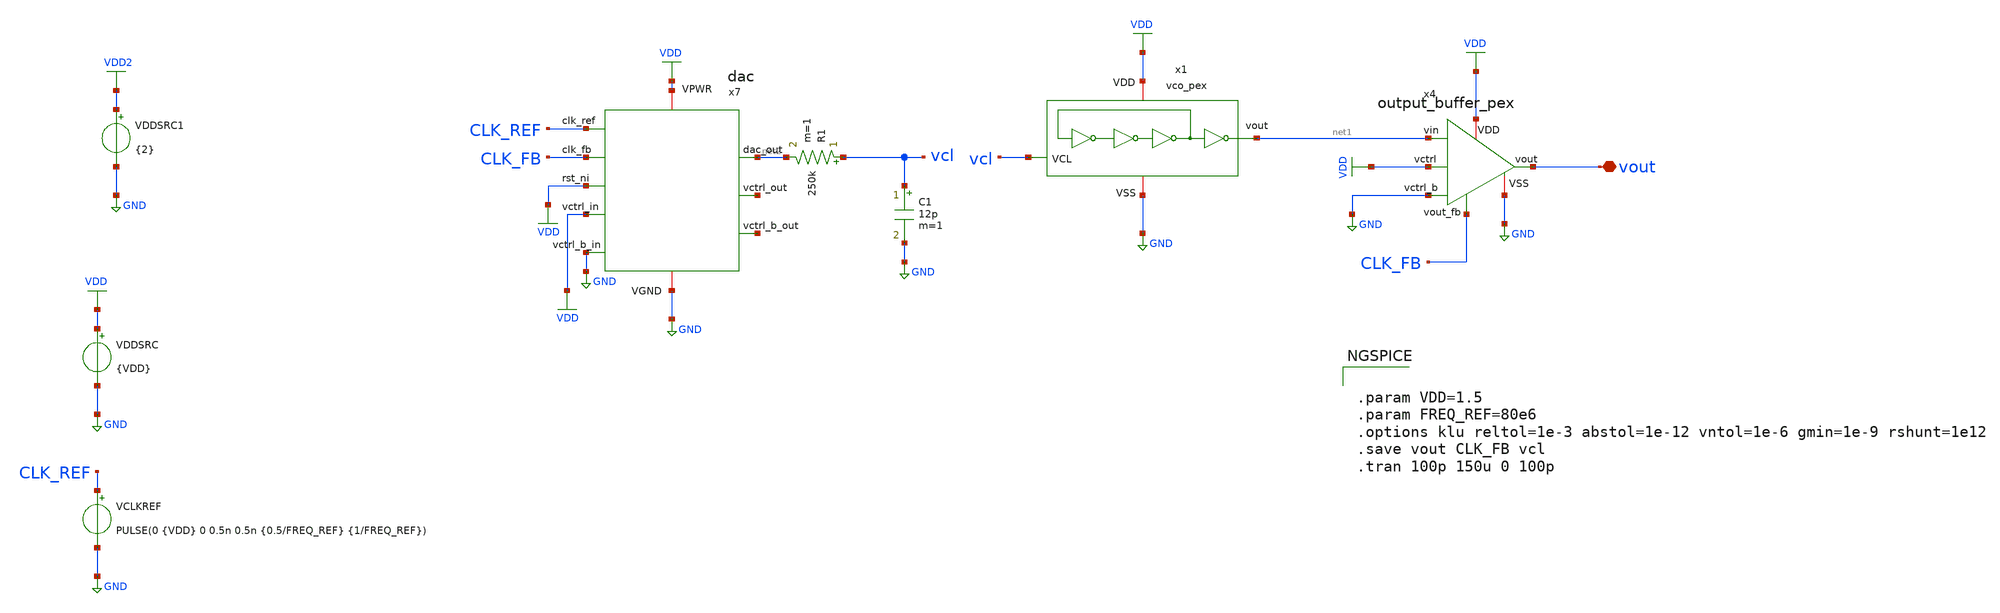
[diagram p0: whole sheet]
** sch_path: macros/heichips26_ook_top/macros/ook_analog_system/testbenches/xschem/dac_tb_tran.sch
**.subckt dac_tb_tran vout
*.iopin vout
VCLKREF CLK_REF GND PULSE(0 {VDD} 0 0.5n 0.5n {0.5/FREQ_REF} {1/FREQ_REF})
VDDSRC VDD GND {VDD}
x4 CLK_FB VDD VDD net1 vout GND GND output_buffer_pex
x1 net1 VDD GND vcl vco_pex
VDDSRC1 VDD2 GND {2}
x7 GND VDD CLK_FB CLK_REF net2 VDD GND net3 VDD net4 dac
R1 vcl net2 250k m=1
C1 vcl GND 12p m=1
**** begin user architecture code


.param VDD=1.5
.param FREQ_REF=80e6
.options klu reltol=1e-3 abstol=1e-12 vntol=1e-6 gmin=1e-9 rshunt=1e12
.save vout CLK_FB vcl
.tran 100p 150u 0 100p



.lib cornerMOSlv.lib mos_tt
.lib cornerMOShv.lib mos_tt
.lib cornerRES.lib res_typ
.lib cornerDIO.lib dio_tt
.lib cornerCAP.lib cap_typ
.include /home/belal/HeiChips/heichips26-on-off/macros/heichips26_ook_top/macros/dac/netlist/xspice/dac.xspice
.include /home/belal/HeiChips/heichips26-on-off/macros/heichips26_ook_top/macros/ook_analog_system/netlist/pex/vco_magic_pex_3.spice
.include /home/belal/HeiChips/heichips26-on-off/macros/heichips26_ook_top/macros/ook_analog_system/netlist/pex/output_buffer_magic_pex_3.spice
.include /home/belal/HeiChips/heichips26-on-off/IHP-Open-PDK/ihp-sg13cmos5l/libs.tech/ngspice/models/cap_mfringe.lib


**** end user architecture code
**.ends
.GLOBAL GND
.GLOBAL VDD
.GLOBAL VDD2
.end
